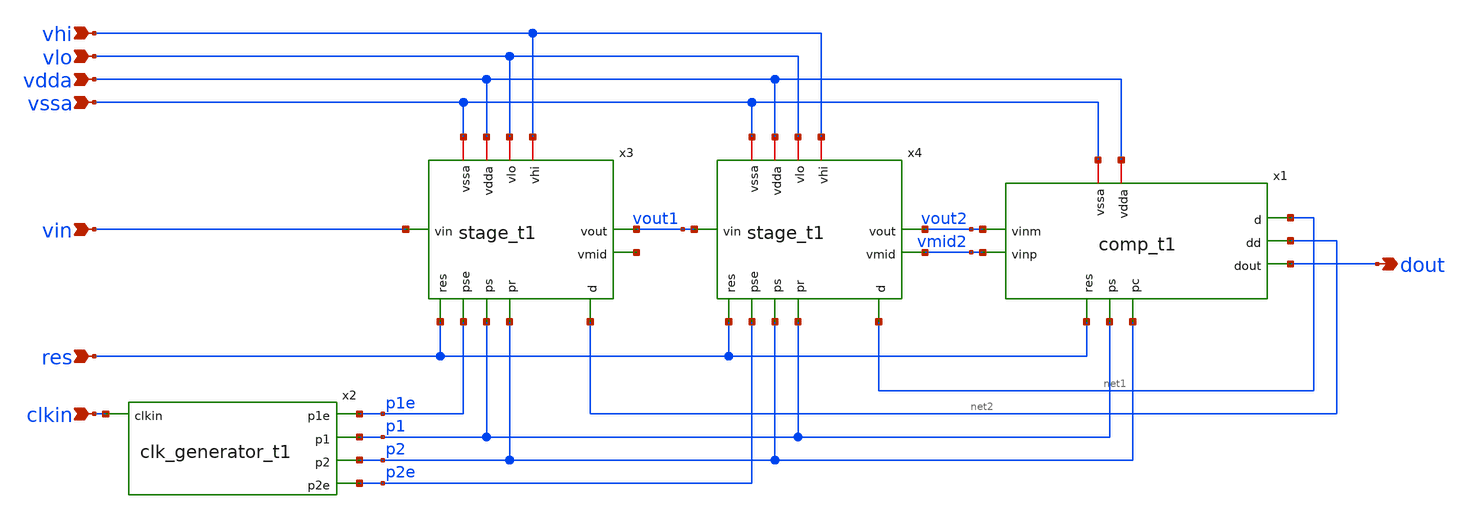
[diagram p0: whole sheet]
** sch_path: 5_Design/4_Layout/Team 1/xschem/IDSM2_t1.sch
* IHP-GmbH/IHP-Open-PDK/ihp-sg13g2/libs.tech/xschem/sg13g2_stdcells/sg13g2_inv_2.sch:
* Copyright 2023 IHP PDK Authors
* Licensed under the Apache License, Version 2.0 (the "License");
**.subckt IDSM2_t1 clkin res vin vssa vdda vlo vhi dout
*.ipin clkin
*.ipin res
*.ipin vin
*.ipin vssa
*.ipin vdda
*.ipin vlo
*.ipin vhi
*.opin dout
x1 vdda p2 net1 net2 vmid2 dout vssa p1 res vout2 comp_t1
x2 p1e clkin p1 p2 p2e clk_generator_t1
x3 res p1e p1 p2 vhi vdda vin vout1 vssa net2 net3 vlo stage_t1
x4 res p2e p2 p1 vhi vdda vout1 vout2 vssa net1 vmid2 vlo stage_t1
**.ends

* expanding   symbol:  //foss/designs/EE628/5_Design/4_Layout/Team 1/xschem/comp_t1.sym # of pins=10
** sym_path: 5_Design/4_Layout/Team 1/xschem/comp_t1.sym
** sch_path: 5_Design/4_Layout/Team 1/xschem/comp_t1.sch
.subckt comp_t1 vdda pc d dd vinp dout vssa ps res vinm
*.ipin pc
*.ipin vinp
*.ipin ps
*.ipin vinm
*.iopin vdda
*.iopin vssa
*.opin d
*.opin dd
*.ipin res
*.opin dout
XM4 vinm_samp ps vinm vssa sg13_lv_nmos w=2u l=0.13u ng=1 m=1 mm_ok=1
XM5 vinm_samp psb vinm vdda sg13_lv_pmos w=6u l=0.13u ng=3 m=1 mm_ok=1
x3 psb ps VDD VSS sg13g2_inv_1
XC1 vinm_samp vssa cap_cmim w=5.77e-6 l=5.77e-6 m=1 mm_ok=1
XM1 out1m pc vdda vdda sg13_lv_pmos w=4u l=0.13u ng=1 m=1 mm_ok=1
XM2 out1m out1p vdda vdda sg13_lv_pmos w=4u l=0.13u ng=1 m=1 mm_ok=1
XM3 out1p out1m vdda vdda sg13_lv_pmos w=4u l=0.13u ng=1 m=1 mm_ok=1
XM6 out1p pc vdda vdda sg13_lv_pmos w=4u l=0.13u ng=1 m=1 mm_ok=1
XM7 out1m out1p d2p vssa sg13_lv_nmos w=2u l=0.13u ng=1 m=1 mm_ok=1
XM8 d2p pc d1p vssa sg13_lv_nmos w=2u l=0.13u ng=1 m=1 mm_ok=1
XM9 d1p vinp vssa vssa sg13_lv_nmos w=2u l=1u ng=1 m=1 mm_ok=1
XM10 out1p out1m d2m vssa sg13_lv_nmos w=2u l=0.13u ng=1 m=1 mm_ok=1
XM11 d2m pc d1m vssa sg13_lv_nmos w=2u l=0.13u ng=1 m=1 mm_ok=1
XM12 d1m vinm_samp vssa vssa sg13_lv_nmos w=2u l=1u ng=1 m=1 mm_ok=1
XM13 net1 out1p VDD VDD sg13_lv_pmos w=4u l=0.13u ng=1 m=1 mm_ok=1
XM14 net1 net2 VDD VDD sg13_lv_pmos w=4u l=0.13u ng=1 m=1 mm_ok=1
XM15 net2 net1 VDD VDD sg13_lv_pmos w=4u l=0.13u ng=1 m=1 mm_ok=1
XM16 net2 out1m VDD VDD sg13_lv_pmos w=4u l=0.13u ng=1 m=1 mm_ok=1
XM17 net1 net2 net3 VSS sg13_lv_nmos w=2u l=0.13u ng=1 m=1 mm_ok=1
XM18 net2 net1 net4 VSS sg13_lv_nmos w=2u l=0.13u ng=1 m=1 mm_ok=1
XM19 net3 out1p VSS VSS sg13_lv_nmos w=2u l=0.13u ng=1 m=1 mm_ok=1
XM20 net4 out1m VSS VSS sg13_lv_nmos w=2u l=0.13u ng=1 m=1 mm_ok=1
x1 d net2 VDD VSS sg13g2_buf_2
x2 dd net6 ps net2 net5 VDD VSS sg13g2_dfrbp_2
x4 net5 res VDD VSS sg13g2_inv_1
x5 dout dd VDD VSS sg13g2_inv_2
.ends


* expanding   symbol:  /foss/designs/EE628/5_Design/4_Layout/Team 1/xschem/clk_generator_t1.sym # of
*+ pins=5
** sym_path: 5_Design/4_Layout/Team 1/xschem/clk_generator_t1.sym
** sch_path: 5_Design/4_Layout/Team 1/xschem/clk_generator_t1.sch
.subckt clk_generator_t1 p1e clkin p1 p2 p2e
*.ipin clkin
*.opin p2e
*.opin p2
*.opin p1
*.opin p1e
x1 clkinb clkin VDD VSS sg13g2_inv_2
x2 net11 clkinbb b2 VDD VSS sg13g2_nand2_2
x3 clkinbb clkinb VDD VSS sg13g2_inv_2
x4 net2 net11 VDD VSS sg13g2_inv_4
x8 net12 b1 clkinb VDD VSS sg13g2_nand2_2
x9 net1 net12 VDD VSS sg13g2_inv_4
x15 net4 net2 VDD VSS sg13g2_inv_4
x16 net3 net1 VDD VSS sg13g2_inv_4
x17 net6 net4 VDD VSS sg13g2_inv_4
x18 net5 net3 VDD VSS sg13g2_inv_4
x19 a1 net6 VDD VSS sg13g2_inv_4
x20 a2 net5 VDD VSS sg13g2_inv_4
x21 p1e a1 VDD VSS sg13g2_inv_4
x22 p2e a2 VDD VSS sg13g2_inv_4
x23 b1 p1e VDD VSS sg13g2_inv_4
x24 b2 p2e VDD VSS sg13g2_inv_4
x25 net7 a1 b1 VDD VSS sg13g2_nand2_2
x26 net8 a2 b2 VDD VSS sg13g2_nand2_2
x5 net9 net7 VDD VSS sg13g2_inv_4
x6 net10 net8 VDD VSS sg13g2_inv_4
x7 p1 net9 VDD VSS sg13g2_inv_8
x10 p2 net10 VDD VSS sg13g2_inv_8
.ends


* expanding   symbol:  /foss/designs/EE628/5_Design/4_Layout/Team 1/xschem/stage_t1.sym # of pins=12
** sym_path: 5_Design/4_Layout/Team 1/xschem/stage_t1.sym
** sch_path: 5_Design/4_Layout/Team 1/xschem/stage_t1.sch
.subckt stage_t1 res pse ps pr vhi vdda vin vout vssa d vmid vlo
*.ipin res
*.ipin pse
*.ipin ps
*.ipin pr
*.iopin vhi
*.ipin vin
*.ipin d
*.iopin vlo
*.iopin vdda
*.iopin vssa
*.opin vout
*.opin vmid
x1 psb ps VDD VSS sg13g2_inv_1
x2 gp d pr VDD VSS sg13g2_nand2b_1
XM2 vout res vx4 vssa sg13_lv_nmos w=2u l=0.13u ng=1 m=1 mm_ok=1
XM3 vx1 gp vhi vdda sg13_lv_pmos w=1.5u l=0.13u ng=1 m=1 mm_ok=1
XM4 vx1 ps vin vssa sg13_lv_nmos w=2u l=0.13u ng=1 m=1 mm_ok=1
XM5 vx1 psb vin vdda sg13_lv_pmos w=6u l=0.13u ng=3 m=1 mm_ok=1
XC2 vx2 vx1 cap_cmim w=5.77e-6 l=5.77e-6 m=1 mm_ok=1
x4 gn pr d VDD VSS sg13g2_and2_1
XM6 vx1 gn vlo vssa sg13_lv_nmos w=0.5u l=0.13u ng=1 m=1 mm_ok=1
XC3 vx3 vx2 cap_cmim w=8.16e-6 l=8.16e-6 m=1 mm_ok=1
XM7 vx4 pr vx2 vssa sg13_lv_nmos w=2u l=0.13u ng=1 m=1 mm_ok=1
XM8 vx4 ps vx3 vssa sg13_lv_nmos w=2u l=0.13u ng=1 m=1 mm_ok=1
XC4 vx4 vout cap_cmim w=8.16e-6 l=8.16e-6 m=1 mm_ok=1
XM9 vx2 pse vmid vssa sg13_lv_nmos w=2u l=0.13u ng=1 m=1 mm_ok=1
XM10 vout vx3 vdda vdda sg13_lv_pmos w=10u l=1.5u ng=4 m=1 mm_ok=1
XM11 vout vx3 vssa vssa sg13_lv_nmos w=2.5u l=1.5u ng=1 m=1 mm_ok=1
XM12 vmid vmid vdda vdda sg13_lv_pmos w=10u l=1.5u ng=4 m=1 mm_ok=1
XM13 vmid vmid vssa vssa sg13_lv_nmos w=2.5u l=1.5u ng=1 m=1 mm_ok=1
.ends


* expanding   symbol:  sg13g2_stdcells/sg13g2_inv_1.sym # of pins=2
** sym_path: sg13g2_stdcells/sg13g2_inv_1.sym
** sch_path: sg13g2_stdcells/sg13g2_inv_1.sch
.subckt sg13g2_inv_1 Y A VDD VSS
*.opin Y
*.ipin A
*.iopin VDD
*.iopin VSS
XM1 Y A VSS VSS sg13_lv_nmos w=740.00n l=130.00n ng=1 m=1 mm_ok=1
XM2 Y A VDD VDD sg13_lv_pmos w=1.12u l=130.00n ng=1 m=1 mm_ok=1
.ends


* expanding   symbol:  sg13g2_stdcells/sg13g2_buf_2.sym # of pins=2
** sym_path: sg13g2_stdcells/sg13g2_buf_2.sym
** sch_path: sg13g2_stdcells/sg13g2_buf_2.sch
.subckt sg13g2_buf_2 X A VDD VSS
*.ipin A
*.opin X
*.iopin VDD
*.iopin VSS
XM1 net1 A VSS VSS sg13_lv_nmos w=640.00n l=130.00n ng=1 m=1 mm_ok=1
XM2 X net1 VSS VSS sg13_lv_nmos w=1.48u l=130.00n ng=2 m=1 mm_ok=1
XM3 net1 A VDD VDD sg13_lv_pmos w=1.000u l=130.00n ng=1 m=1 mm_ok=1
XM4 X net1 VDD VDD sg13_lv_pmos w=2.24u l=130.00n ng=2 m=1 mm_ok=1
.ends


* expanding   symbol:  sg13g2_stdcells/sg13g2_dfrbp_2.sym # of pins=5
** sym_path: sg13g2_stdcells/sg13g2_dfrbp_2.sym
** sch_path: sg13g2_stdcells/sg13g2_dfrbp_2.sch
.subckt sg13g2_dfrbp_2 Q Q_N CLK D RESET_B VDD VSS
*.ipin D
*.ipin RESET_B
*.ipin CLK
*.opin Q
*.opin Q_N
*.iopin VDD
*.iopin VSS
XM1 Db D net12 VSS sg13_lv_nmos w=420.00n l=130.00n ng=1 m=1 mm_ok=1
XM2 net12 RESET_B VSS VSS sg13_lv_nmos w=420.00n l=130.00n ng=1 m=1 mm_ok=1
XM3 net2 clkneg net11 VSS sg13_lv_nmos w=420.00n l=130.00n ng=1 m=1 mm_ok=1
XM4 net11 net3 VSS VSS sg13_lv_nmos w=420.00n l=130.00n ng=1 m=1 mm_ok=1
XM5 net3 net2 net7 VSS sg13_lv_nmos w=420.00n l=130.00n ng=1 m=1 mm_ok=1
XM6 net7 RESET_B VSS VSS sg13_lv_nmos w=420.00n l=130.00n ng=1 m=1 mm_ok=1
XM7 Q_N net2 VSS VSS sg13_lv_nmos w=1.48u l=130.00n ng=2 m=1 mm_ok=1
XM8 net1 net2 VSS VSS sg13_lv_nmos w=640.00n l=130.00n ng=1 m=1 mm_ok=1
XM9 Q net1 VSS VSS sg13_lv_nmos w=1.48u l=130.00n ng=2 m=1 mm_ok=1
XM10 clkneg CLK VSS VSS sg13_lv_nmos w=740.00n l=130.00n ng=1 m=1 mm_ok=1
XM11 clkpos clkneg VSS VSS sg13_lv_nmos w=740.00n l=130.00n ng=1 m=1 mm_ok=1
XM12 Db clkneg net4 VSS sg13_lv_nmos w=420.00n l=130.00n ng=1 m=1 mm_ok=1
XM13 net4 clkpos net10 VSS sg13_lv_nmos w=420.00n l=130.00n ng=1 m=1 mm_ok=1
XM14 net10 net5 net6 VSS sg13_lv_nmos w=420.00n l=130.00n ng=1 m=1 mm_ok=1
XM15 net6 RESET_B VSS VSS sg13_lv_nmos w=420.00n l=130.00n ng=1 m=1 mm_ok=1
XM16 net5 net4 VSS VSS sg13_lv_nmos w=740.00n l=130.00n ng=1 m=1 mm_ok=1
XM17 net5 clkpos net2 VSS sg13_lv_nmos w=740.00n l=130.00n ng=1 m=1 mm_ok=1
XM18 Db RESET_B VDD VDD sg13_lv_pmos w=420.00n l=130.00n ng=1 m=1 mm_ok=1
XM19 Db D VDD VDD sg13_lv_pmos w=420.00n l=130.00n ng=1 m=1 mm_ok=1
XM20 net9 net3 VDD VDD sg13_lv_pmos w=420.00n l=130.00n ng=1 m=1 mm_ok=1
XM21 net2 clkpos net9 VDD sg13_lv_pmos w=420.00n l=130.00n ng=1 m=1 mm_ok=1
XM22 net3 net2 VDD VDD sg13_lv_pmos w=420.00n l=130.00n ng=1 m=1 mm_ok=1
XM23 net3 RESET_B VDD VDD sg13_lv_pmos w=420.00n l=130.00n ng=1 m=1 mm_ok=1
XM24 Q_N net2 VDD VDD sg13_lv_pmos w=2.24u l=130.00n ng=2 m=1 mm_ok=1
XM25 net1 net2 VDD VDD sg13_lv_pmos w=1.000u l=130.00n ng=1 m=1 mm_ok=1
XM26 Q net1 VDD VDD sg13_lv_pmos w=2.24u l=130.00n ng=2 m=1 mm_ok=1
XM27 clkneg CLK VDD VDD sg13_lv_pmos w=1.12u l=130.00n ng=1 m=1 mm_ok=1
XM28 clkpos clkneg VDD VDD sg13_lv_pmos w=1.12u l=130.00n ng=1 m=1 mm_ok=1
XM29 Db clkpos net4 VDD sg13_lv_pmos w=420.00n l=130.00n ng=1 m=1 mm_ok=1
XM30 net8 net5 VDD VDD sg13_lv_pmos w=420.00n l=130.00n ng=1 m=1 mm_ok=1
XM31 net4 clkneg net8 VDD sg13_lv_pmos w=420.00n l=130.00n ng=1 m=1 mm_ok=1
XM32 net4 RESET_B VDD VDD sg13_lv_pmos w=420.00n l=130.00n ng=1 m=1 mm_ok=1
XM33 net5 net4 VDD VDD sg13_lv_pmos w=1.000u l=130.00n ng=1 m=1 mm_ok=1
XM34 net5 clkneg net2 VDD sg13_lv_pmos w=1.000u l=130.00n ng=1 m=1 mm_ok=1
.ends


* expanding   symbol:  sg13g2_stdcells/sg13g2_inv_2.sym # of pins=2
** sym_path: sg13g2_stdcells/sg13g2_inv_2.sym
** sch_path: sg13g2_stdcells/sg13g2_inv_2.sch
.subckt sg13g2_inv_2 Y A VDD VSS
*.opin Y
*.ipin A
*.iopin VDD
*.iopin VSS
XM1 Y A VSS VSS sg13_lv_nmos w=1.48u l=130.00n ng=2 m=1 mm_ok=1
XM2 Y A VDD VDD sg13_lv_pmos w=2.24u l=130.00n ng=2 m=1 mm_ok=1
.ends


* expanding   symbol:  sg13g2_stdcells/sg13g2_nand2_2.sym # of pins=3
** sym_path: sg13g2_stdcells/sg13g2_nand2_2.sym
** sch_path: sg13g2_stdcells/sg13g2_nand2_2.sch
.subckt sg13g2_nand2_2 Y A B VDD VSS
*.iopin VDD
*.iopin VSS
*.opin Y
*.ipin B
*.ipin A
XM1 Y A net1 VSS sg13_lv_nmos w=1.44u l=130.00n ng=2 m=1 mm_ok=1
XM2 net1 B VSS VSS sg13_lv_nmos w=1.44u l=130.00n ng=2 m=1 mm_ok=1
XM3 Y A VDD VDD sg13_lv_pmos w=2.24u l=130.00n ng=2 m=1 mm_ok=1
XM4 Y B VDD VDD sg13_lv_pmos w=2.24u l=130.00n ng=2 m=1 mm_ok=1
.ends


* expanding   symbol:  sg13g2_stdcells/sg13g2_inv_4.sym # of pins=2
** sym_path: sg13g2_stdcells/sg13g2_inv_4.sym
** sch_path: sg13g2_stdcells/sg13g2_inv_4.sch
.subckt sg13g2_inv_4 Y A VDD VSS
*.ipin A
*.opin Y
*.iopin VDD
*.iopin VSS
XM1 Y A VSS VSS sg13_lv_nmos w=2.96u l=130.00n ng=4 m=1 mm_ok=1
XM2 Y A VDD VDD sg13_lv_pmos w=4.48u l=130.00n ng=4 m=1 mm_ok=1
.ends


* expanding   symbol:  sg13g2_stdcells/sg13g2_inv_8.sym # of pins=2
** sym_path: sg13g2_stdcells/sg13g2_inv_8.sym
** sch_path: sg13g2_stdcells/sg13g2_inv_8.sch
.subckt sg13g2_inv_8 Y A VDD VSS
*.opin Y
*.ipin A
*.iopin VDD
*.iopin VSS
XM1 Y A VSS VSS sg13_lv_nmos w=5.92u l=130.00n ng=8 m=1 mm_ok=1
XM2 Y A VDD VDD sg13_lv_pmos w=8.96u l=130.00n ng=8 m=1 mm_ok=1
.ends


* expanding   symbol:  sg13g2_stdcells/sg13g2_nand2b_1.sym # of pins=3
** sym_path: sg13g2_stdcells/sg13g2_nand2b_1.sym
** sch_path: sg13g2_stdcells/sg13g2_nand2b_1.sch
.subckt sg13g2_nand2b_1 Y A_N B VDD VSS
*.opin Y
*.ipin B
*.ipin A_N
*.iopin VDD
*.iopin VSS
XM1 net1 A_N VSS VSS sg13_lv_nmos w=550.00n l=130.00n ng=1 m=1 mm_ok=1
XM2 Y net1 net2 VSS sg13_lv_nmos w=740.00n l=130.00n ng=1 m=1 mm_ok=1
XM3 net2 B VSS VSS sg13_lv_nmos w=740.00n l=130.00n ng=1 m=1 mm_ok=1
XM4 Y B VDD VDD sg13_lv_pmos w=1.12u l=130.00n ng=1 m=1 mm_ok=1
XM5 net1 A_N VDD VDD sg13_lv_pmos w=840.00n l=130.00n ng=1 m=1 mm_ok=1
XM6 Y net1 VDD VDD sg13_lv_pmos w=1.12u l=130.00n ng=1 m=1 mm_ok=1
.ends


* expanding   symbol:  sg13g2_stdcells/sg13g2_and2_1.sym # of pins=3
** sym_path: sg13g2_stdcells/sg13g2_and2_1.sym
** sch_path: sg13g2_stdcells/sg13g2_and2_1.sch
.subckt sg13g2_and2_1 X A B VDD VSS
*.ipin A
*.ipin B
*.opin X
*.iopin VDD
*.iopin VSS
XM1 net1 A net2 VSS sg13_lv_nmos w=640.00n l=130.00n ng=1 m=1 mm_ok=1
XM2 net2 B VSS VSS sg13_lv_nmos w=640.00n l=130.00n ng=1 m=1 mm_ok=1
XM3 X net1 VSS VSS sg13_lv_nmos w=740.00n l=130.00n ng=1 m=1 mm_ok=1
XM4 net1 B VDD VDD sg13_lv_pmos w=840.00n l=130.00n ng=1 m=1 mm_ok=1
XM5 net1 A VDD VDD sg13_lv_pmos w=840.00n l=130.00n ng=1 m=1 mm_ok=1
XM6 X net1 VDD VDD sg13_lv_pmos w=1.12u l=130.00n ng=1 m=1 mm_ok=1
.ends

.GLOBAL VDD
.GLOBAL VSS
.end
